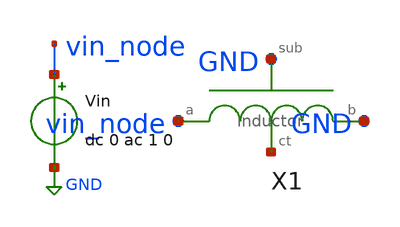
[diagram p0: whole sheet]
** sch_path: tb/inductor/tb_yparam.sch
**.subckt tb_yparam
X1 net1 vin_node GND GND inductor
Vin vin_node GND dc 0 ac 1 0
**** begin user architecture code


.include 'models_dir'/design.spice
.option TEMP='temperature'
.option warn=1
.control
save all
ac dec 100 1meg 20g
let y11 = i(vin)/v(vin_node)
let y11_re = real(y11)
let y11_im = imag(y11)
set wr_singlescale
wrdata 'simpath'/'filename'_'N'.data frequency y11_re y11_im
quit
.endc


**** end user architecture code
**.ends
.GLOBAL GND
.end
